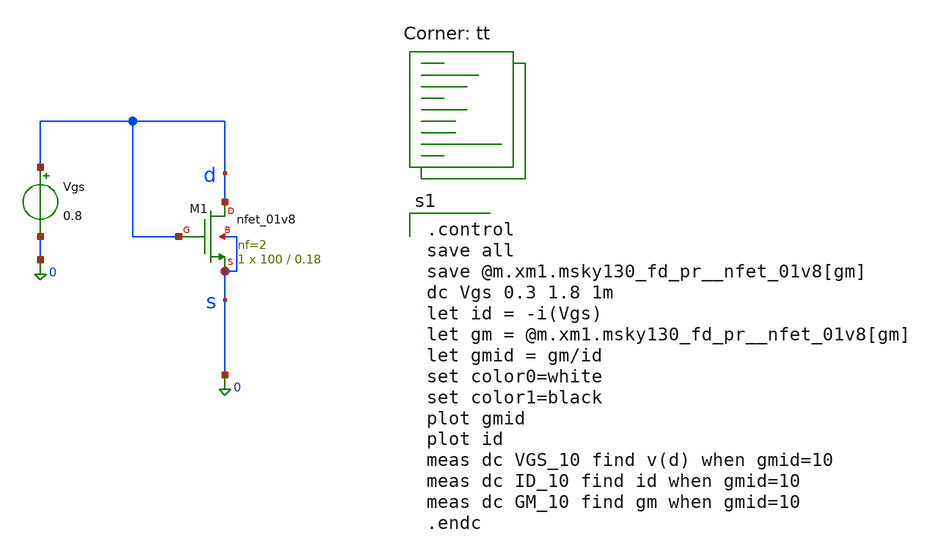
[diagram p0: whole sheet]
** sch_path: Homework 6 - Simulation on Open Source Softwares/Simulations/ex3_gmid.sch
**.subckt ex3_gmid
XM1 d d 0 0 sky130_fd_pr__nfet_01v8 L=0.18 W=100 nf=2 ad='int((2 + 1)/2) * 100 / 2 * 0.29' as='int((2 + 2)/2) * 100 / 2 * 0.29'
+ pd='2*int((2 + 1)/2) * (100 / 2 + 0.29)' ps='2*int((2 + 2)/2) * (100 / 2 + 0.29)' nrd='0.29 / 100 ' nrs='0.29 / 100 '
+ sa=0 sb=0 sd=0 mult=1 m=1
Vgs d 0 0.8
**** begin user architecture code
.lib $::SKYWATER_MODELS/sky130.lib.spice tt

.control
save all
save @m.xm1.msky130_fd_pr__nfet_01v8[gm]
dc Vgs 0.3 1.8 1m
let id = -i(Vgs)
let gm = @m.xm1.msky130_fd_pr__nfet_01v8[gm]
let gmid = gm/id
set color0=white
set color1=black
plot gmid
plot id
meas dc VGS_10 find v(d) when gmid=10
meas dc ID_10 find id when gmid=10
meas dc GM_10 find gm when gmid=10
.endc

**** end user architecture code
**.ends
.end
